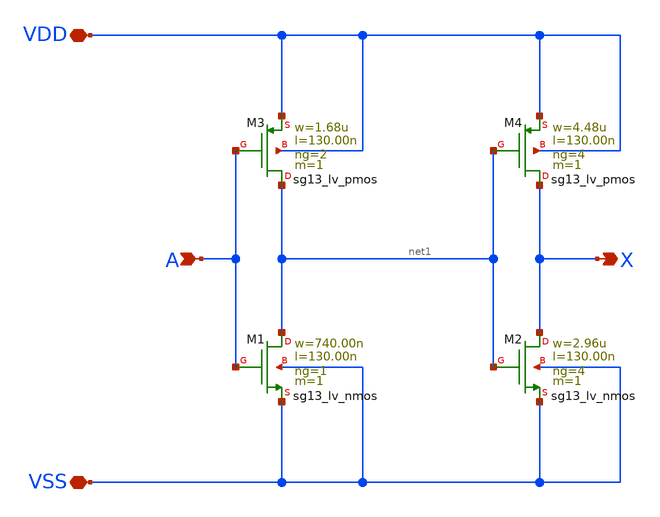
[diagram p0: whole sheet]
** sch_path: ihp-sg13g2/libs.tech/xschem/sg13g2_stdcells/sg13g2_buf_4.sch
* Copyright 2023 IHP PDK Authors
* Licensed under the Apache License, Version 2.0 (the "License");
* you may not use this file except in compliance with the License.
* You may obtain a copy of the License at
* https://www.apache.org/licenses/LICENSE-2.0
* Unless required by applicable law or agreed to in writing, software
* distributed under the License is distributed on an "AS IS" BASIS,
* WITHOUT WARRANTIES OR CONDITIONS OF ANY KIND, either express or implied.
* See the License for the specific language governing permissions and
* limitations under the License.
**.subckt sg13g2_buf_4 A X VDD VSS
*.ipin A
*.opin X
*.iopin VDD
*.iopin VSS
XM1 net1 A VSS VSS sg13_lv_nmos w=740.00n l=130.00n ng=1 m=1 mm_ok=1
XM2 X net1 VSS VSS sg13_lv_nmos w=2.96u l=130.00n ng=4 m=1 mm_ok=1
XM3 net1 A VDD VDD sg13_lv_pmos w=1.68u l=130.00n ng=2 m=1 mm_ok=1
XM4 X net1 VDD VDD sg13_lv_pmos w=4.48u l=130.00n ng=4 m=1 mm_ok=1
**.ends
.end
